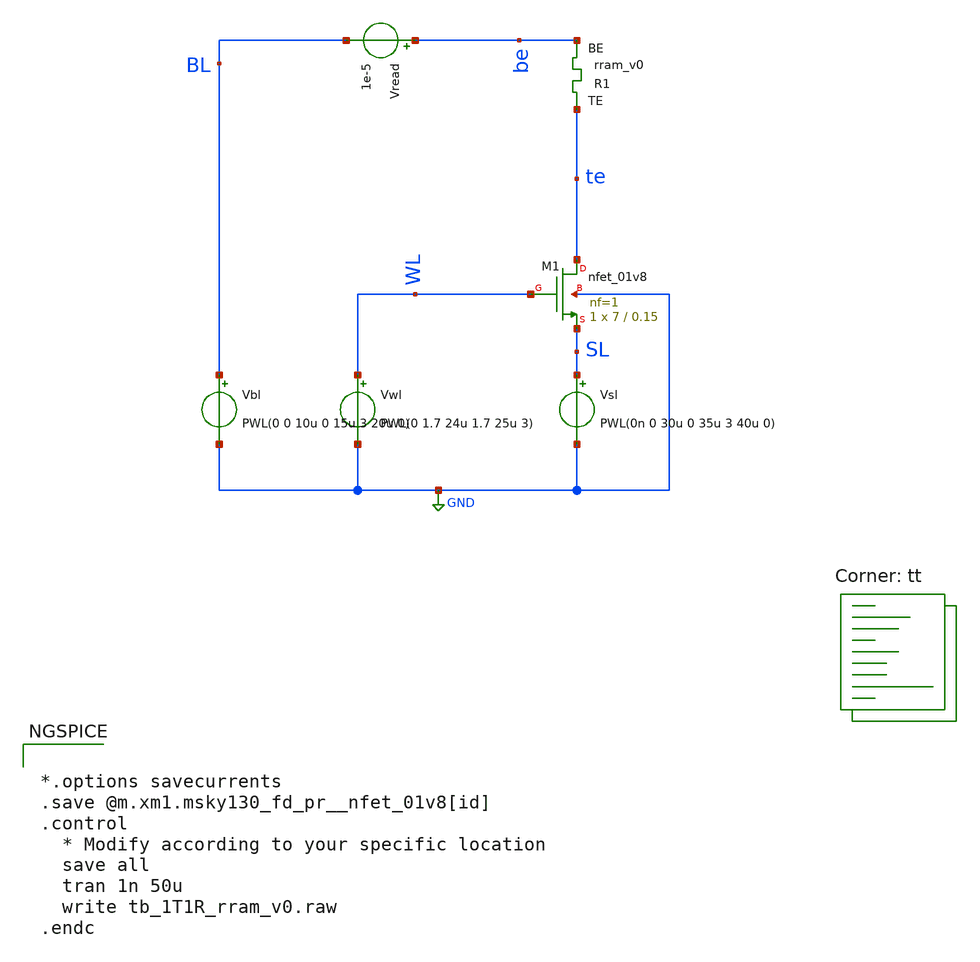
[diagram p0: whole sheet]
** sch_path: memristor_models/wellposed/tb_1T1R_rram_v0.sch
**.subckt tb_1T1R_rram_v0
XM1 te WL SL GND sky130_fd_pr__nfet_01v8 L=0.15 W=7 nf=1 ad='int((nf+1)/2) * W/nf * 0.29' as='int((nf+2)/2) * W/nf * 0.29'
+ pd='2*int((nf+1)/2) * (W/nf + 0.29)' ps='2*int((nf+2)/2) * (W/nf + 0.29)' nrd='0.29 / W' nrs='0.29 / W'
+ sa=0 sb=0 sd=0 mult=1 m=1
Vwl WL GND PWL(0 1.7 24u 1.7 25u 3)
Vbl BL GND PWL(0 0 10u 0 15u 3 20u 0)
Vread be BL 1e-5
Vsl SL GND PWL(0n 0 30u 0 35u 3 40u 0)
XR1 te be rram_v0
**** begin user architecture code


*.options savecurrents
.save @m.xm1.msky130_fd_pr__nfet_01v8[id]
.control
  * Modify according to your specific location
  save all
  tran 1n 50u
  write tb_1T1R_rram_v0.raw
.endc



.lib $::SKYWATER_MODELS/sky130.lib.spice tt

** opencircuitdesign pdks install
.inc $::SKYWATER_MODELS/rram_v0.spice

**** end user architecture code
**.ends
.GLOBAL GND
.end
